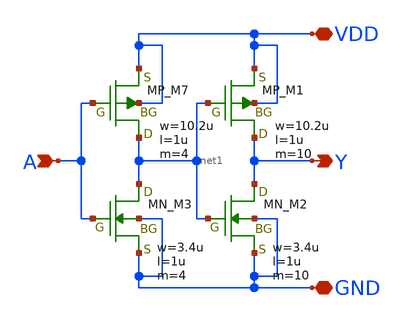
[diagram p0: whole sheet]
** sch_path: libs.tech/xschem/TR-1um_5_stdcell/CLKBUF_X2.sch
**.subckt CLKBUF_X2 A Y VDD GND
*.ipin A
*.opin Y
*.iopin VDD
*.iopin GND
XM7 net1 A VDD VDD PMOS w=10.2u l=1u nrd=0 nrs=0 m=4
XM1 Y net1 VDD VDD PMOS w=10.2u l=1u nrd=0 nrs=0 m=10
XM3 net1 A GND GND NMOS w=3.4u l=1u nrd=0 nrs=0 m=4
XM2 Y net1 GND GND NMOS w=3.4u l=1u nrd=0 nrs=0 m=10
**.ends
.end
